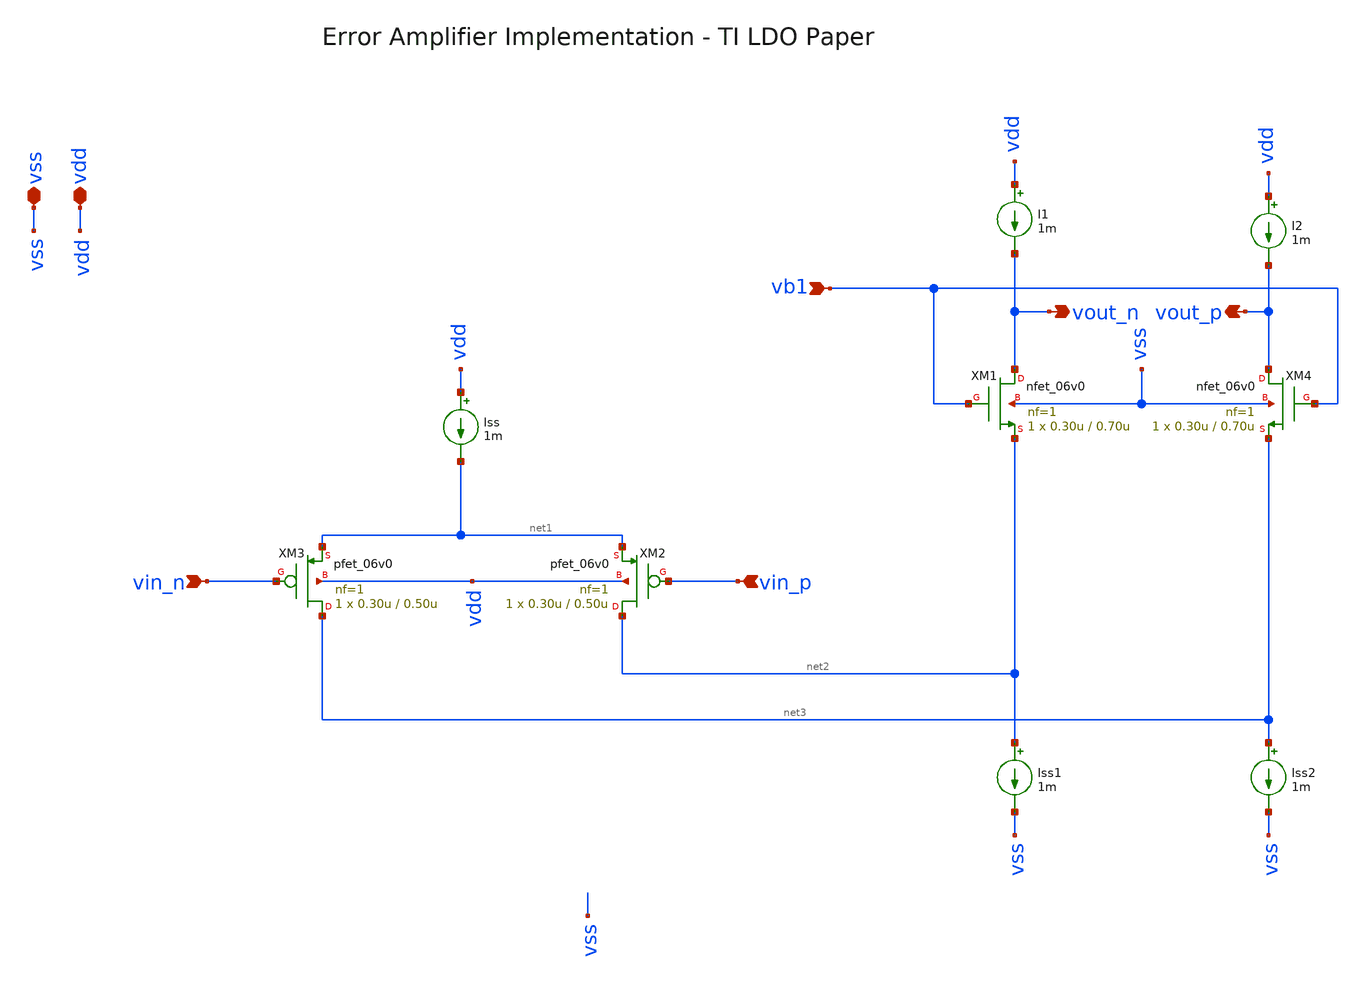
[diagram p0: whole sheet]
** sch_path: analog-db/circuits/ldo_005_buffered_ref/reference/ti-ldo/gen_amps/foldded_cascode_pmos_input.sch
**.subckt foldded_cascode_pmos_input vdd vss vin_n vin_p vb1 vout_n vout_p
*.iopin vdd
*.iopin vss
*.ipin vin_n
*.ipin vin_p
*.ipin vb1
*.opin vout_n
*.opin vout_p
Iss vdd net1 1m
Iss1 net2 vss 1m
Iss2 net3 vss 1m
XM3 net3 vin_n net1 vdd pfet_06v0 L=0.50u W=0.30u nf=1 ad='int((nf+1)/2) * W/nf * 0.18u' as='int((nf+2)/2) * W/nf * 0.18u'
+ pd='2*int((nf+1)/2) * (W/nf + 0.18u)' ps='2*int((nf+2)/2) * (W/nf + 0.18u)' nrd='0.18u / W' nrs='0.18u / W'
+ sa=0 sb=0 sd=0 m=1
XM1 vout_n vb1 net2 vss nfet_06v0 L=0.70u W=0.30u nf=1 ad='int((nf+1)/2) * W/nf * 0.18u' as='int((nf+2)/2) * W/nf * 0.18u'
+ pd='2*int((nf+1)/2) * (W/nf + 0.18u)' ps='2*int((nf+2)/2) * (W/nf + 0.18u)' nrd='0.18u / W' nrs='0.18u / W'
+ sa=0 sb=0 sd=0 m=1
XM2 net2 vin_p net1 vdd pfet_06v0 L=0.50u W=0.30u nf=1 ad='int((nf+1)/2) * W/nf * 0.18u' as='int((nf+2)/2) * W/nf * 0.18u'
+ pd='2*int((nf+1)/2) * (W/nf + 0.18u)' ps='2*int((nf+2)/2) * (W/nf + 0.18u)' nrd='0.18u / W' nrs='0.18u / W'
+ sa=0 sb=0 sd=0 m=1
XM4 vout_p vb1 net3 vss nfet_06v0 L=0.70u W=0.30u nf=1 ad='int((nf+1)/2) * W/nf * 0.18u' as='int((nf+2)/2) * W/nf * 0.18u'
+ pd='2*int((nf+1)/2) * (W/nf + 0.18u)' ps='2*int((nf+2)/2) * (W/nf + 0.18u)' nrd='0.18u / W' nrs='0.18u / W'
+ sa=0 sb=0 sd=0 m=1
I1 vdd vout_n 1m
I2 vdd vout_p 1m
**.ends
.end
